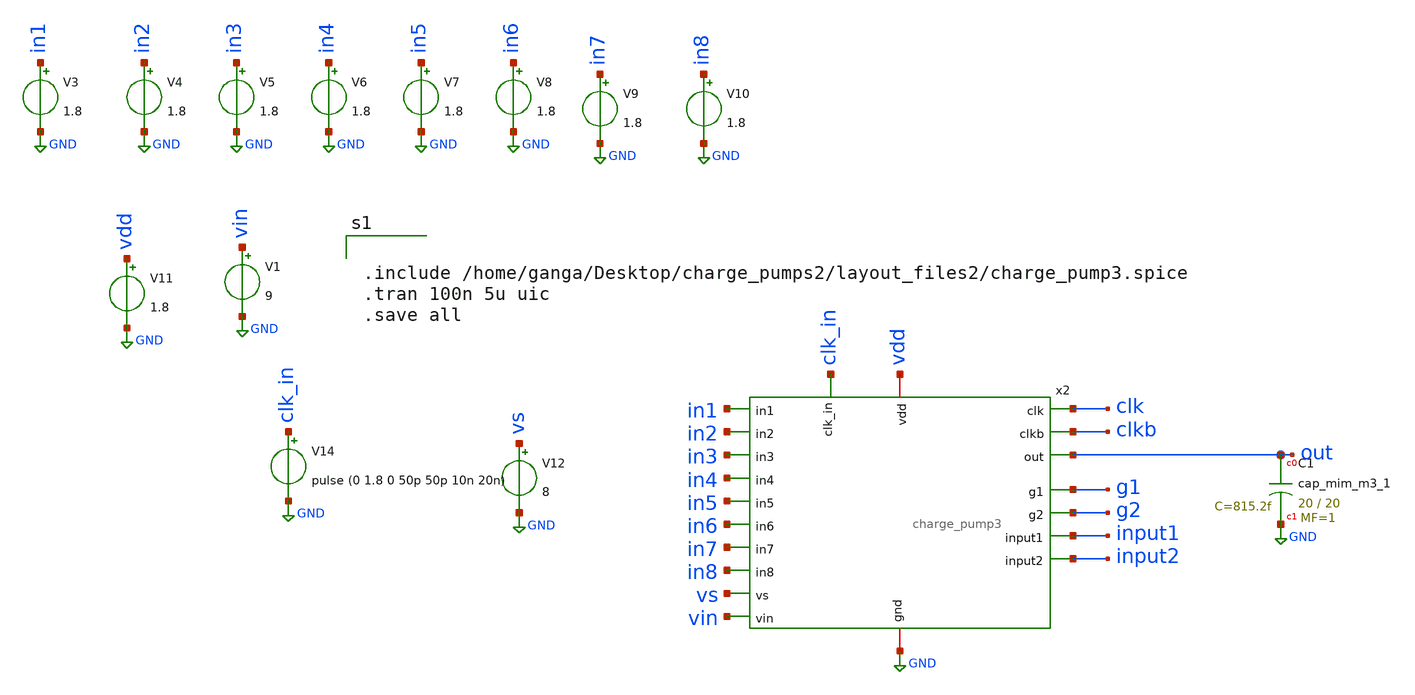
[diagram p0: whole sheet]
** sch_path: xschem/charge_pumps2/CP2_post_layout.sch
**.subckt CP2_post_layout
V1 vin GND 9
V3 in1 GND 1.8
V4 in2 GND 1.8
V5 in3 GND 1.8
V6 in4 GND 1.8
V7 in5 GND 1.8
V8 in6 GND 1.8
V9 in7 GND 1.8
V10 in8 GND 1.8
V11 vdd GND 1.8
V12 vs GND 8
XC1 out GND sky130_fd_pr__cap_mim_m3_1 W=20 L=20 MF=1 m=1
x2 in7 g2 vin g1 clk_in input1 input2 vdd GND in1 in2 in3 in4 in5 in6 in8 vs clk clkb charge_pump3
V14 clk_in GND pulse (0 1.8 0 50p 50p 10n 20n)
**** begin user architecture code

** opencircuitdesign pdks install
.lib $::SKYWATER_MODELS/sky130.lib.spice tt




.include /home/ganga/Desktop/charge_pumps2/layout_files2/charge_pump3.spice
.tran 100n 5u uic
.save all


**** end user architecture code
**.ends
.GLOBAL GND
.end
